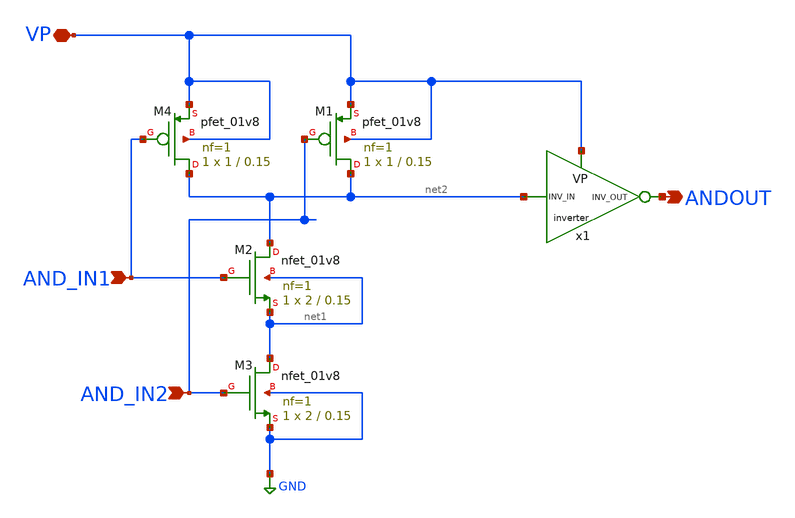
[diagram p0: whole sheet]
** sch_path: AllSymbols&Sch/Gates/StaticAndGate.sch
**.subckt StaticAndGate AND_IN1 ANDOUT AND_IN2 VP
*.ipin AND_IN1
*.opin ANDOUT
*.ipin AND_IN2
*.iopin VP
XM1 net2 AND_IN2 VP VP sky130_fd_pr__pfet_01v8 L=0.15 W=1 nf=1 ad='int((1 + 1)/2) * 1 / 1 * 0.29' as='int((1 + 2)/2) * 1 / 1 * 0.29'
+ pd='2*int((1 + 1)/2) * (1 / 1 + 0.29)' ps='2*int((1 + 2)/2) * (1 / 1 + 0.29)' nrd='0.29 / 1 ' nrs='0.29 / 1 '
+ sa=0 sb=0 sd=0 mult=1 m=1
XM2 net2 AND_IN1 net1 net1 sky130_fd_pr__nfet_01v8 L=0.15 W=2 nf=1 ad='int((1 + 1)/2) * 2 / 1 * 0.29'
+ as='int((1 + 2)/2) * 2 / 1 * 0.29' pd='2*int((1 + 1)/2) * (2 / 1 + 0.29)' ps='2*int((1 + 2)/2) * (2 / 1 + 0.29)'
+ nrd='0.29 / 2 ' nrs='0.29 / 2 ' sa=0 sb=0 sd=0 mult=1 m=1
XM3 net1 AND_IN2 GND GND sky130_fd_pr__nfet_01v8 L=0.15 W=2 nf=1 ad='int((1 + 1)/2) * 2 / 1 * 0.29' as='int((1 + 2)/2) * 2 / 1 * 0.29'
+ pd='2*int((1 + 1)/2) * (2 / 1 + 0.29)' ps='2*int((1 + 2)/2) * (2 / 1 + 0.29)' nrd='0.29 / 2 ' nrs='0.29 / 2 '
+ sa=0 sb=0 sd=0 mult=1 m=1
XM4 net2 AND_IN1 VP VP sky130_fd_pr__pfet_01v8 L=0.15 W=1 nf=1 ad='int((1 + 1)/2) * 1 / 1 * 0.29' as='int((1 + 2)/2) * 1 / 1 * 0.29'
+ pd='2*int((1 + 1)/2) * (1 / 1 + 0.29)' ps='2*int((1 + 2)/2) * (1 / 1 + 0.29)' nrd='0.29 / 1 ' nrs='0.29 / 1 '
+ sa=0 sb=0 sd=0 mult=1 m=1
x1 VP ANDOUT net2 inverter
**.ends

* expanding   symbol:
*+  /home/safal/projects/GitHub_CMOS_4bit_ALU/AllSymbols&Sch/GenericSym/inverter.sym # of pins=3
** sym_path: AllSymbols&Sch/GenericSym/inverter.sym
** sch_path: AllSymbols&Sch/GenericSym/inverter.sch
.subckt inverter VP inv_out inv_in
*.ipin inv_in
*.opin inv_out
*.iopin VP
XM1 inv_out inv_in VP VP sky130_fd_pr__pfet_01v8 L=0.15 W=2 nf=1 ad='int((1 + 1)/2) * 2 / 1 * 0.29' as='int((1 + 2)/2) * 2 / 1 * 0.29'
+ pd='2*int((1 + 1)/2) * (2 / 1 + 0.29)' ps='2*int((1 + 2)/2) * (2 / 1 + 0.29)' nrd='0.29 / 2 ' nrs='0.29 / 2 '
+ sa=0 sb=0 sd=0 mult=1 m=1
XM2 inv_out inv_in GND GND sky130_fd_pr__nfet_01v8 L=0.15 W=1 nf=1 ad='int((1 + 1)/2) * 1 / 1 * 0.29'
+ as='int((1 + 2)/2) * 1 / 1 * 0.29' pd='2*int((1 + 1)/2) * (1 / 1 + 0.29)' ps='2*int((1 + 2)/2) * (1 / 1 + 0.29)'
+ nrd='0.29 / 1 ' nrs='0.29 / 1 ' sa=0 sb=0 sd=0 mult=1 m=1
.ends

.GLOBAL GND
.end
